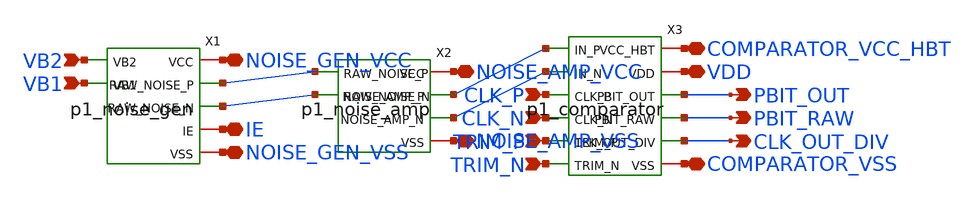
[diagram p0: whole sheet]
** sch_path: designs/p1-pbit/top/source-backed-v2/p1_top.sch
**.subckt p1_top PBIT_OUT PBIT_RAW CLK_OUT_DIV CLK_P CLK_N TRIM_P TRIM_N NOISE_GEN_VCC NOISE_GEN_VSS
*+ NOISE_AMP_VCC NOISE_AMP_VSS COMPARATOR_VCC_HBT VDD COMPARATOR_VSS VB1 VB2 IE
*.opin PBIT_OUT
*.opin PBIT_RAW
*.opin CLK_OUT_DIV
*.ipin CLK_P
*.ipin CLK_N
*.ipin TRIM_P
*.ipin TRIM_N
*.iopin NOISE_GEN_VCC
*.iopin NOISE_GEN_VSS
*.iopin NOISE_AMP_VCC
*.iopin NOISE_AMP_VSS
*.iopin COMPARATOR_VCC_HBT
*.iopin VDD
*.iopin COMPARATOR_VSS
*.ipin VB1
*.ipin VB2
*.iopin IE
X1 net1 net2 NOISE_GEN_VCC NOISE_GEN_VSS VB1 VB2 IE p1_noise_gen
X2 net3 net4 net1 net2 NOISE_AMP_VCC NOISE_AMP_VSS p1_noise_amp
X3 PBIT_OUT PBIT_RAW CLK_OUT_DIV net3 net4 CLK_P CLK_N TRIM_P TRIM_N COMPARATOR_VCC_HBT VDD
+ COMPARATOR_VSS p1_comparator
**.ends
.end
